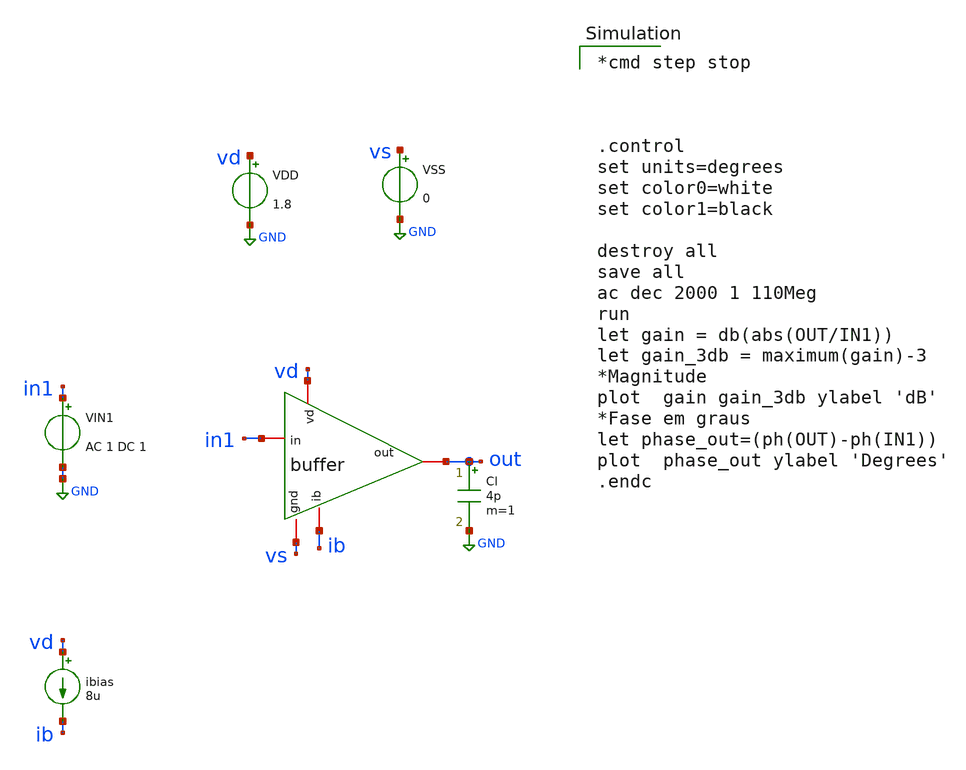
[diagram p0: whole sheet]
** sch_path: amp-op/xschem/buffer_tb-ac.sch
* Copyright 2020 Stefan Frederik Schippers
* Licensed under the Apache License, Version 2.0 (the "License");
* you may not use this file except in compliance with the License.
* You may obtain a copy of the License at
* https://www.apache.org/licenses/LICENSE-2.0
* Unless required by applicable law or agreed to in writing, software
* distributed under the License is distributed on an "AS IS" BASIS,
* WITHOUT WARRANTIES OR CONDITIONS OF ANY KIND, either express or implied.
* See the License for the specific language governing permissions and
* limitations under the License.
**.subckt buffer_tb-ac
VIN1 in1 GND AC 1 DC 1
ibias vd ib 8u
VDD vd GND 1.8
VSS vs GND 0
Cl out GND 4p m=1
X1 vd in1 out ib vs buffer
**** begin user architecture code

*cmd step stop



.control
set units=degrees
set color0=white
set color1=black

destroy all
save all
ac dec 2000 1 110Meg
run
let gain = db(abs(OUT/IN1))
let gain_3db = maximum(gain)-3
*Magnitude
plot  gain gain_3db ylabel 'dB'
*Fase em graus
let phase_out=(ph(OUT)-ph(IN1))
plot  phase_out ylabel 'Degrees'
.endc

 .lib $::SKYWATER_MODELS/sky130.lib.spice tt
.include $::SKYWATER_STDCELLS/sky130_fd_sc_hd.spice

**** end user architecture code
**.ends

* expanding   symbol:  /home/hugodg/projects-sky130/temp-sensor/amp-op/xschem/buffer.sym # of pins=5
** sym_path: buffer/xschem/buffer.sym
** sch_path: buffer/xschem/buffer.sch
.subckt buffer vd in out ib gnd
*.iopin vd
*.iopin ib
*.iopin out
*.iopin in
*.iopin gnd
XM3 net2 net2 vd vd sky130_fd_pr__pfet_01v8 L=1 W=1 nf=1 ad='int((nf+1)/2) * W/nf * 0.29' as='int((nf+2)/2) * W/nf * 0.29'
+ pd='2*int((nf+1)/2) * (W/nf + 0.29)' ps='2*int((nf+2)/2) * (W/nf + 0.29)' nrd='0.29 / W' nrs='0.29 / W'
+ sa=0 sb=0 sd=0 mult=1 m=1
XM1 net2 out net4 gnd sky130_fd_pr__nfet_01v8 L=1 W=10 nf=10 ad='int((nf+1)/2) * W/nf * 0.29' as='int((nf+2)/2) * W/nf * 0.29'
+ pd='2*int((nf+1)/2) * (W/nf + 0.29)' ps='2*int((nf+2)/2) * (W/nf + 0.29)' nrd='0.29 / W' nrs='0.29 / W'
+ sa=0 sb=0 sd=0 mult=1 m=1
XM2 net3 in net4 gnd sky130_fd_pr__nfet_01v8 L=1 W=10 nf=10 ad='int((nf+1)/2) * W/nf * 0.29' as='int((nf+2)/2) * W/nf * 0.29'
+ pd='2*int((nf+1)/2) * (W/nf + 0.29)' ps='2*int((nf+2)/2) * (W/nf + 0.29)' nrd='0.29 / W' nrs='0.29 / W'
+ sa=0 sb=0 sd=0 mult=1 m=1
XM4 net3 net3 vd vd sky130_fd_pr__pfet_01v8 L=1 W=1 nf=1 ad='int((nf+1)/2) * W/nf * 0.29' as='int((nf+2)/2) * W/nf * 0.29'
+ pd='2*int((nf+1)/2) * (W/nf + 0.29)' ps='2*int((nf+2)/2) * (W/nf + 0.29)' nrd='0.29 / W' nrs='0.29 / W'
+ sa=0 sb=0 sd=0 mult=1 m=1
XM5 net4 ib gnd gnd sky130_fd_pr__nfet_01v8 L=1 W=1 nf=1 ad='int((nf+1)/2) * W/nf * 0.29' as='int((nf+2)/2) * W/nf * 0.29'
+ pd='2*int((nf+1)/2) * (W/nf + 0.29)' ps='2*int((nf+2)/2) * (W/nf + 0.29)' nrd='0.29 / W' nrs='0.29 / W'
+ sa=0 sb=0 sd=0 mult=1 m=1
XM6 out net3 vd vd sky130_fd_pr__pfet_01v8 L=1 W=10 nf=10 ad='int((nf+1)/2) * W/nf * 0.29' as='int((nf+2)/2) * W/nf * 0.29'
+ pd='2*int((nf+1)/2) * (W/nf + 0.29)' ps='2*int((nf+2)/2) * (W/nf + 0.29)' nrd='0.29 / W' nrs='0.29 / W'
+ sa=0 sb=0 sd=0 mult=1 m=1
XM7 out net1 gnd gnd sky130_fd_pr__nfet_01v8 L=1 W=10 nf=10 ad='int((nf+1)/2) * W/nf * 0.29' as='int((nf+2)/2) * W/nf * 0.29'
+ pd='2*int((nf+1)/2) * (W/nf + 0.29)' ps='2*int((nf+2)/2) * (W/nf + 0.29)' nrd='0.29 / W' nrs='0.29 / W'
+ sa=0 sb=0 sd=0 mult=1 m=1
XM8 net1 net2 vd vd sky130_fd_pr__pfet_01v8 L=1 W=10 nf=10 ad='int((nf+1)/2) * W/nf * 0.29' as='int((nf+2)/2) * W/nf * 0.29'
+ pd='2*int((nf+1)/2) * (W/nf + 0.29)' ps='2*int((nf+2)/2) * (W/nf + 0.29)' nrd='0.29 / W' nrs='0.29 / W'
+ sa=0 sb=0 sd=0 mult=1 m=1
XM9 net1 net1 gnd gnd sky130_fd_pr__nfet_01v8 L=1 W=10 nf=10 ad='int((nf+1)/2) * W/nf * 0.29' as='int((nf+2)/2) * W/nf * 0.29'
+ pd='2*int((nf+1)/2) * (W/nf + 0.29)' ps='2*int((nf+2)/2) * (W/nf + 0.29)' nrd='0.29 / W' nrs='0.29 / W'
+ sa=0 sb=0 sd=0 mult=1 m=1
XM10 ib ib gnd gnd sky130_fd_pr__nfet_01v8 L=1 W=1 nf=1 ad='int((nf+1)/2) * W/nf * 0.29' as='int((nf+2)/2) * W/nf * 0.29'
+ pd='2*int((nf+1)/2) * (W/nf + 0.29)' ps='2*int((nf+2)/2) * (W/nf + 0.29)' nrd='0.29 / W' nrs='0.29 / W'
+ sa=0 sb=0 sd=0 mult=1 m=1
XPD1 net8 net7 net6 net5 sky130_fd_pr__pfet_01v8 L=1 W=1 nf=1 ad='int((nf+1)/2) * W/nf * 0.29' as='int((nf+2)/2) * W/nf * 0.29'
+ pd='2*int((nf+1)/2) * (W/nf + 0.29)' ps='2*int((nf+2)/2) * (W/nf + 0.29)' nrd='0.29 / W' nrs='0.29 / W'
+ sa=0 sb=0 sd=0 mult=1 m=1
XPD2 net12 net11 net10 net9 sky130_fd_pr__pfet_01v8 L=1 W=1 nf=1 ad='int((nf+1)/2) * W/nf * 0.29' as='int((nf+2)/2) * W/nf * 0.29'
+ pd='2*int((nf+1)/2) * (W/nf + 0.29)' ps='2*int((nf+2)/2) * (W/nf + 0.29)' nrd='0.29 / W' nrs='0.29 / W'
+ sa=0 sb=0 sd=0 mult=1 m=1
XPD3 net16 net15 net14 net13 sky130_fd_pr__pfet_01v8 L=1 W=1 nf=1 ad='int((nf+1)/2) * W/nf * 0.29' as='int((nf+2)/2) * W/nf * 0.29'
+ pd='2*int((nf+1)/2) * (W/nf + 0.29)' ps='2*int((nf+2)/2) * (W/nf + 0.29)' nrd='0.29 / W' nrs='0.29 / W'
+ sa=0 sb=0 sd=0 mult=1 m=1
XPD4 net20 net19 net18 net17 sky130_fd_pr__pfet_01v8 L=1 W=1 nf=1 ad='int((nf+1)/2) * W/nf * 0.29' as='int((nf+2)/2) * W/nf * 0.29'
+ pd='2*int((nf+1)/2) * (W/nf + 0.29)' ps='2*int((nf+2)/2) * (W/nf + 0.29)' nrd='0.29 / W' nrs='0.29 / W'
+ sa=0 sb=0 sd=0 mult=1 m=1
XND1 net25 net21 net26 gnd sky130_fd_pr__nfet_01v8 L=1 W=1 nf=1 ad='int((nf+1)/2) * W/nf * 0.29' as='int((nf+2)/2) * W/nf * 0.29'
+ pd='2*int((nf+1)/2) * (W/nf + 0.29)' ps='2*int((nf+2)/2) * (W/nf + 0.29)' nrd='0.29 / W' nrs='0.29 / W'
+ sa=0 sb=0 sd=0 mult=1 m=1
XND2 net27 net22 net28 gnd sky130_fd_pr__nfet_01v8 L=1 W=1 nf=1 ad='int((nf+1)/2) * W/nf * 0.29' as='int((nf+2)/2) * W/nf * 0.29'
+ pd='2*int((nf+1)/2) * (W/nf + 0.29)' ps='2*int((nf+2)/2) * (W/nf + 0.29)' nrd='0.29 / W' nrs='0.29 / W'
+ sa=0 sb=0 sd=0 mult=1 m=1
XND3 net29 net23 net30 gnd sky130_fd_pr__nfet_01v8 L=1 W=1 nf=1 ad='int((nf+1)/2) * W/nf * 0.29' as='int((nf+2)/2) * W/nf * 0.29'
+ pd='2*int((nf+1)/2) * (W/nf + 0.29)' ps='2*int((nf+2)/2) * (W/nf + 0.29)' nrd='0.29 / W' nrs='0.29 / W'
+ sa=0 sb=0 sd=0 mult=1 m=1
XND4 net32 net24 net31 gnd sky130_fd_pr__nfet_01v8 L=1 W=1 nf=1 ad='int((nf+1)/2) * W/nf * 0.29' as='int((nf+2)/2) * W/nf * 0.29'
+ pd='2*int((nf+1)/2) * (W/nf + 0.29)' ps='2*int((nf+2)/2) * (W/nf + 0.29)' nrd='0.29 / W' nrs='0.29 / W'
+ sa=0 sb=0 sd=0 mult=1 m=1
.ends

.GLOBAL GND
.end
